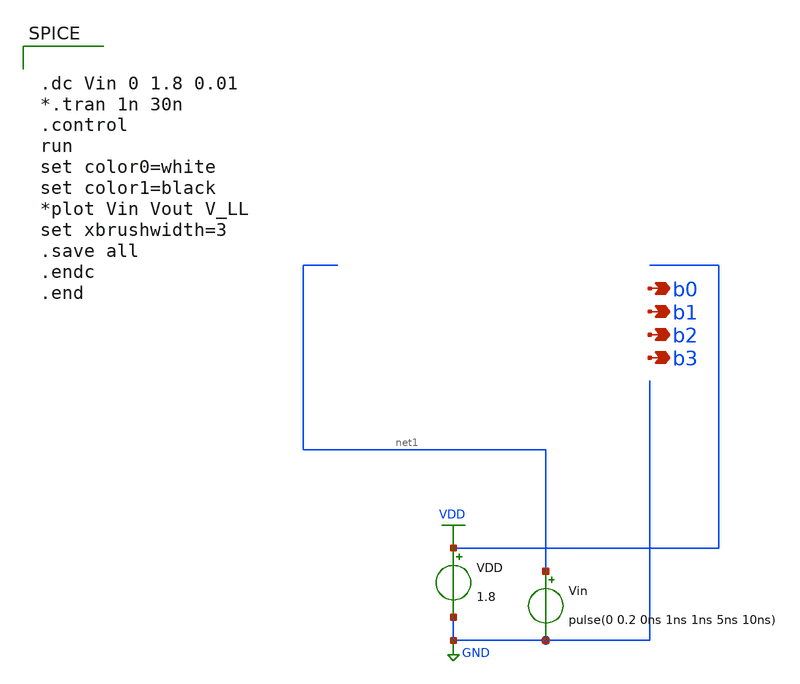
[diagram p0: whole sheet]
** sch_path: xschem/Vth_sch/Pre_layout/Analog_with_sub.sch
**.subckt Analog_with_sub b0 b1 b2 b3
*.opin b0
*.opin b1
*.opin b2
*.opin b3
VDD VDD GND 1.8
Vin net1 GND pulse(0 0.2 0ns 1ns 1ns 5ns 10ns)
**** begin user architecture code


.lib /usr/local/share/pdk/sky130A/libs.tech/ngspice/sky130.lib.spice tt
.include /usr/local/share/pdk/sky130A/libs.ref/sky130_fd_sc_hd/spice/sky130_fd_sc_hd.spice
.save all





.dc Vin 0 1.8 0.01
*.tran 1n 30n
.control
run
set color0=white
set color1=black
*plot Vin Vout V_LL
set xbrushwidth=3
.save all
.endc
.end


**** end user architecture code
**.ends
.GLOBAL VDD
.GLOBAL GND
.end
